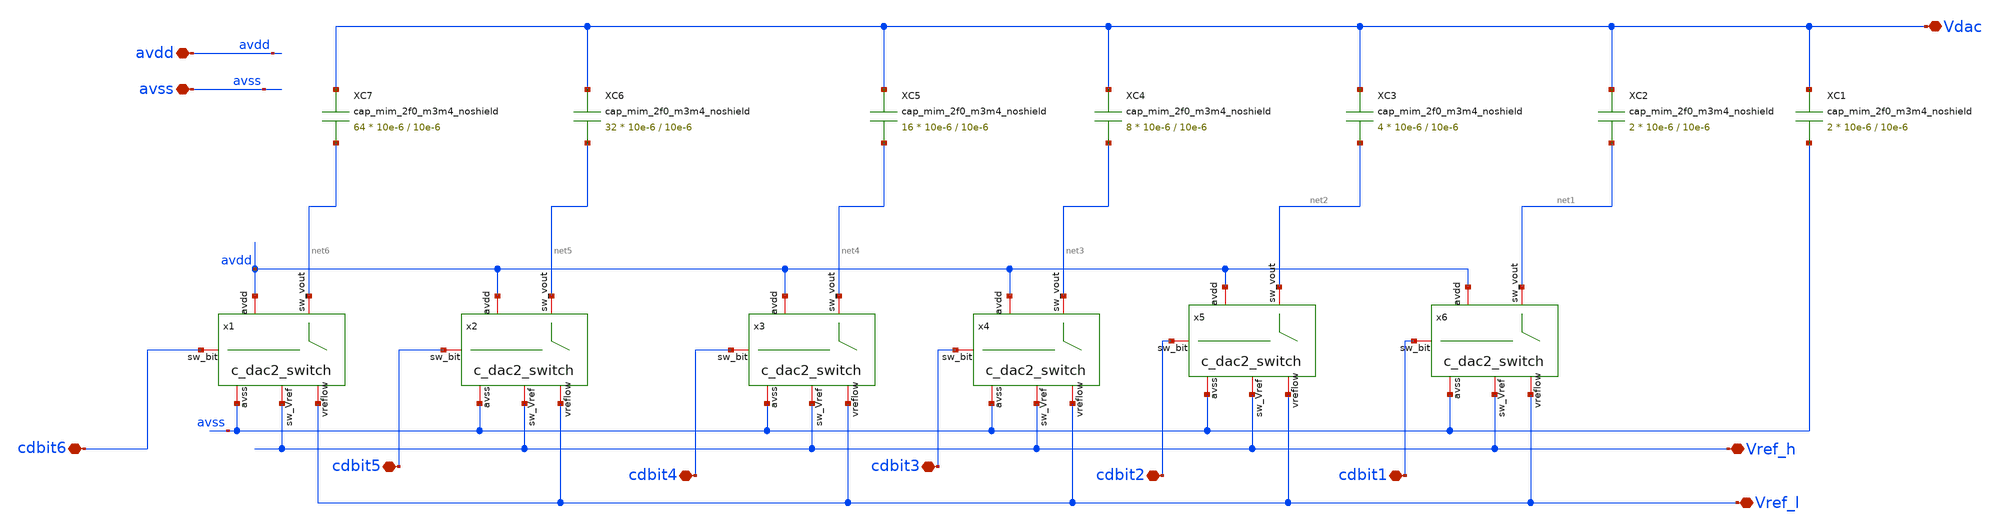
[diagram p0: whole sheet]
** sch_path: designs/libs/WK_Kadam/6bit_CDAC_V2_CO_MK.sch
**.subckt 6bit_CDAC_V2_CO_MK Vref_h Vdac avdd avss cdbit6 cdbit5 cdbit4 cdbit3 cdbit2 cdbit1 Vref_l
*.iopin Vref_h
*.iopin Vdac
*.iopin avdd
*.iopin avss
*.iopin cdbit6
*.iopin cdbit5
*.iopin cdbit4
*.iopin cdbit3
*.iopin cdbit2
*.iopin cdbit1
*.iopin Vref_l
XC3 Vdac net2 cap_mim_2f0_m3m4_noshield c_width=10e-6 c_length=10e-6 m=4
XC4 Vdac net3 cap_mim_2f0_m3m4_noshield c_width=10e-6 c_length=10e-6 m=8
XC5 Vdac net4 cap_mim_2f0_m3m4_noshield c_width=10e-6 c_length=10e-6 m=16
XC6 Vdac net5 cap_mim_2f0_m3m4_noshield c_width=10e-6 c_length=10e-6 m=32
XC7 Vdac net6 cap_mim_2f0_m3m4_noshield c_width=10e-6 c_length=10e-6 m=64
XC1 Vdac avss cap_mim_2f0_m3m4_noshield c_width=10e-6 c_length=10e-6 m=2
XC2 Vdac net1 cap_mim_2f0_m3m4_noshield c_width=10e-6 c_length=10e-6 m=2
x1 net6 cdbit6 avss avdd Vref_h Vref_l c_dac2_switch
x2 net5 cdbit5 avss avdd Vref_h Vref_l c_dac2_switch
x3 net4 cdbit4 avss avdd Vref_h Vref_l c_dac2_switch
x4 net3 cdbit3 avss avdd Vref_h Vref_l c_dac2_switch
x5 net2 cdbit2 avss avdd Vref_h Vref_l c_dac2_switch
x6 net1 cdbit1 avss avdd Vref_h Vref_l c_dac2_switch
**.ends

* expanding   symbol:  libs/WK_Kadam/c_dac2_switch.sym # of pins=6
** sym_path: designs/libs/WK_Kadam/c_dac2_switch.sym
** sch_path: designs/libs/WK_Kadam/c_dac2_switch.sch
.subckt c_dac2_switch sw_vout sw_bit avss avdd sw_Vref vreflow
*.iopin avdd
*.iopin avss
*.iopin sw_bit
*.iopin sw_vout
*.iopin sw_Vref
*.iopin vreflow
XM1 sw_vout sw_bit sw_Vref avss nfet_03v3 L=0.28u W=2u nf=1 ad='int((nf+1)/2) * W/nf * 0.18u' as='int((nf+2)/2) * W/nf * 0.18u'
+ pd='2*int((nf+1)/2) * (W/nf + 0.18u)' ps='2*int((nf+2)/2) * (W/nf + 0.18u)' nrd='0.18u / W' nrs='0.18u / W'
+ sa=0 sb=0 sd=0 m=1
XM3 sw_vout net1 vreflow avss nfet_03v3 L=0.28u W=2u nf=1 ad='int((nf+1)/2) * W/nf * 0.18u' as='int((nf+2)/2) * W/nf * 0.18u'
+ pd='2*int((nf+1)/2) * (W/nf + 0.18u)' ps='2*int((nf+2)/2) * (W/nf + 0.18u)' nrd='0.18u / W' nrs='0.18u / W'
+ sa=0 sb=0 sd=0 m=1
XM4 vreflow sw_bit sw_vout avdd pfet_03v3 L=0.28u W=2u nf=1 ad='int((nf+1)/2) * W/nf * 0.18u' as='int((nf+2)/2) * W/nf * 0.18u'
+ pd='2*int((nf+1)/2) * (W/nf + 0.18u)' ps='2*int((nf+2)/2) * (W/nf + 0.18u)' nrd='0.18u / W' nrs='0.18u / W'
+ sa=0 sb=0 sd=0 m=1
XM2 sw_Vref net1 sw_vout avdd pfet_03v3 L=0.28u W=2u nf=1 ad='int((nf+1)/2) * W/nf * 0.18u' as='int((nf+2)/2) * W/nf * 0.18u'
+ pd='2*int((nf+1)/2) * (W/nf + 0.18u)' ps='2*int((nf+2)/2) * (W/nf + 0.18u)' nrd='0.18u / W' nrs='0.18u / W'
+ sa=0 sb=0 sd=0 m=1
x1v avdd sw_bit net1 avss inv_test
.ends


* expanding   symbol:  libs/WK_Kadam/inv_test.sym # of pins=4
** sym_path: libs/WK_Kadam/inv_test.sym
** sch_path: libs/WK_Kadam/inv_test.sch
.subckt inv_test avdd in out avss
*.iopin avdd
*.iopin avss
*.iopin in
*.iopin out
XM3 out in avss avss nfet_03v3 L=0.28u W=1u nf=1 ad='int((nf+1)/2) * W/nf * 0.18u' as='int((nf+2)/2) * W/nf * 0.18u'
+ pd='2*int((nf+1)/2) * (W/nf + 0.18u)' ps='2*int((nf+2)/2) * (W/nf + 0.18u)' nrd='0.18u / W' nrs='0.18u / W'
+ sa=0 sb=0 sd=0 m=1
XM4 out in avdd avdd pfet_03v3 L=0.28u W=2.5u nf=1 ad='int((nf+1)/2) * W/nf * 0.18u' as='int((nf+2)/2) * W/nf * 0.18u'
+ pd='2*int((nf+1)/2) * (W/nf + 0.18u)' ps='2*int((nf+2)/2) * (W/nf + 0.18u)' nrd='0.18u / W' nrs='0.18u / W'
+ sa=0 sb=0 sd=0 m=1
.ends

.end
